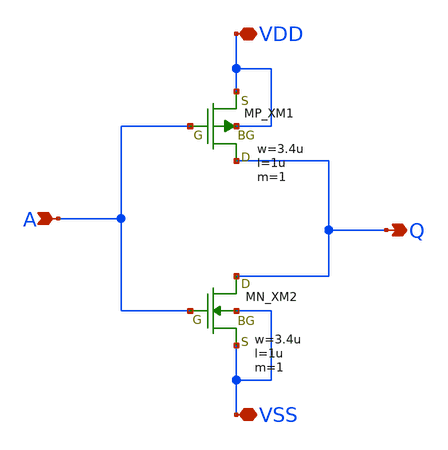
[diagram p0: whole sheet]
** sch_path: schematic/20250924_OSS_Workshop/Qdai/inverter_MUX_02/inv_LiBo.sch
**.subckt inv_LiBo VSS VDD Q A
*.iopin VSS
*.iopin VDD
*.opin Q
*.ipin A
XXM1 Q A VDD VDD PMOS w=3.4u l=1u nrd=0 nrs=0 m=1
XXM2 Q A VSS VSS NMOS w=3.4u l=1u nrd=0 nrs=0 m=1
**.ends
.end
